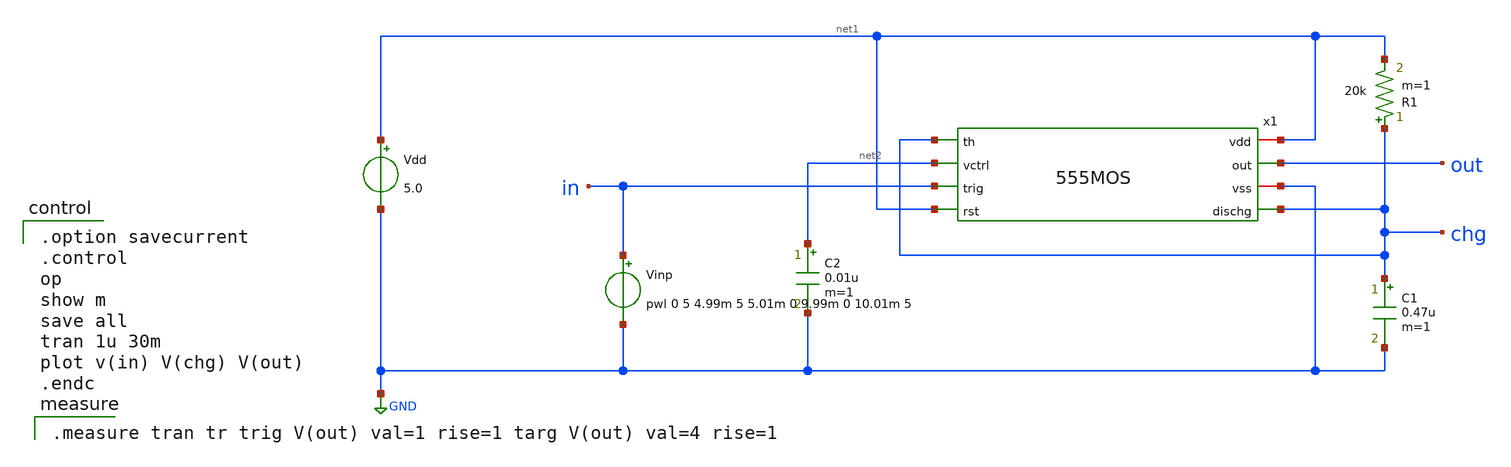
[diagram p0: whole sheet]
** sch_path: member_project/555timer/makoto645/555MOS_tran.sch
**.subckt 555MOS_tran
Vdd net1 GND 5.0
C1 chg GND 0.47u m=1
R1 chg net1 20k m=1
Vinp in GND pwl 0 5 4.99m 5 5.01m 0 9.99m 0 10.01m 5
x1 net1 chg out net2 in GND net1 chg 555MOS
C2 net2 GND 0.01u m=1
**** begin user architecture code

.option savecurrent
.control
op
show m
save all
tran 1u 30m
plot v(in) V(chg) V(out)
.endc


.measure tran tr trig V(out) val=1 rise=1 targ V(out) val=4 rise=1

 .include $::LIB/ip62_models
**** end user architecture code
**.ends

* expanding   symbol:  555MOS.sym # of pins=8
** sym_path: member_project/555timer/makoto645/555MOS.sym
** sch_path: member_project/555timer/makoto645/555MOS.sch
.subckt 555MOS vdd th out vctrl trig vss rst dischg
*.ipin vctrl
*.opin out
*.ipin trig
*.ipin th
*.ipin rst
*.opin dischg
*.iopin vdd
*.iopin vss
XM2 net2 vctrl net5 vss NMOS w=20u l=2u as=0 ad=0 ps=0 pd=0 nrd=0 nrs=0 m=1
XM1 net1 th net5 vss NMOS w=20u l=2u as=0 ad=0 ps=0 pd=0 nrd=0 nrs=0 m=1
XM3 net1 net1 vdd vdd PMOS w=20u l=2u as=0 ad=0 ps=0 pd=0 nrd=0 nrs=0 m=1
XM4 net4 net1 vdd vdd PMOS w=20u l=2u as=0 ad=0 ps=0 pd=0 nrd=0 nrs=0 m=1
XM5 net3 net2 vdd vdd PMOS w=20u l=2u as=0 ad=0 ps=0 pd=0 nrd=0 nrs=0 m=1
XM6 net2 net2 vdd vdd PMOS w=20u l=2u as=0 ad=0 ps=0 pd=0 nrd=0 nrs=0 m=1
XM7 net7 net11 net6 vdd PMOS w=80u l=2u as=0 ad=0 ps=0 pd=0 nrd=0 nrs=0 m=1
XR2 vdd net6 vdd F_RR w=6e-06 l=13.2e-06 R=1 tc1=0 tc2=0 m=1
XM8 net8 trig net7 vdd PMOS w=40u l=2u as=0 ad=0 ps=0 pd=0 nrd=0 nrs=0 m=1
XM9 net9 net10 net7 vdd PMOS w=40u l=2u as=0 ad=0 ps=0 pd=0 nrd=0 nrs=0 m=1
XM10 net8 net9 vss vss NMOS w=20u l=2u as=0 ad=0 ps=0 pd=0 nrd=0 nrs=0 m=1
XM11 net9 net9 vss vss NMOS w=20u l=2u as=0 ad=0 ps=0 pd=0 nrd=0 nrs=0 m=1
XR3 vdd vctrl vdd F_RR w=4e-06 l=42e-06 R=1 tc1=0 tc2=0 m=1
XR4 vctrl net10 vdd F_RR w=4e-06 l=42e-06 R=1 tc1=0 tc2=0 m=1
XR5 net10 vss vdd F_RR w=4e-06 l=42e-06 R=1 tc1=0 tc2=0 m=1
XM12 net3 net3 vss vss NMOS w=20u l=2u as=0 ad=0 ps=0 pd=0 nrd=0 nrs=0 m=1
XM13 net4 net3 vss vss NMOS w=20u l=2u as=0 ad=0 ps=0 pd=0 nrd=0 nrs=0 m=1
XM14 net11 net11 vdd vdd PMOS w=40u l=2u as=0 ad=0 ps=0 pd=0 nrd=0 nrs=0 m=1
XM15 net15 net11 vdd vdd PMOS w=40u l=2u as=0 ad=0 ps=0 pd=0 nrd=0 nrs=0 m=1
XM16 net12 net4 net13 vss NMOS w=20u l=2u as=0 ad=0 ps=0 pd=0 nrd=0 nrs=0 m=1
XM17 net12 net12 net14 vss NMOS w=20u l=2u as=0 ad=0 ps=0 pd=0 nrd=0 nrs=0 m=1
XR6 net11 net12 vdd F_RR w=4e-06 l=24.6e-06 R=1 tc1=0 tc2=0 m=1
XM18 net13 net8 vss vss NMOS w=20u l=2u as=0 ad=0 ps=0 pd=0 nrd=0 nrs=0 m=1
XM19 net14 net13 vss vss NMOS w=20u l=2u as=0 ad=0 ps=0 pd=0 nrd=0 nrs=0 m=1
XM20 net15 net14 vss vss NMOS w=20u l=2u as=0 ad=0 ps=0 pd=0 nrd=0 nrs=0 m=1
XM21 net16 net15 net18 vss NMOS w=20u l=2u as=0 ad=0 ps=0 pd=0 nrd=0 nrs=0 m=1
XR7 net15 net13 vdd F_RR w=4e-06 l=23.5e-06 R=1 tc1=0 tc2=0 m=1
XR8 vdd net16 vdd F_RR w=4e-06 l=24.6e-06 R=1 tc1=0 tc2=0 m=1
XM24 vdd net17 out vss NMOS w=40u l=2u as=0 ad=0 ps=0 pd=0 nrd=0 nrs=0 m=1
XM25 out net18 vss vss NMOS w=40u l=2u as=0 ad=0 ps=0 pd=0 nrd=0 nrs=0 m=1
XM22 vdd net16 net17 vss NMOS w=20u l=2u as=0 ad=0 ps=0 pd=0 nrd=0 nrs=0 m=1
XM23 vss net16 out vdd PMOS w=40u l=2u as=0 ad=0 ps=0 pd=0 nrd=0 nrs=0 m=1
XR9 net17 out vdd F_RR w=4e-06 l=24.6e-06 R=1 tc1=0 tc2=0 m=1
XR10 net18 vss vdd F_RR w=4e-06 l=24.6e-06 R=1 tc1=0 tc2=0 m=1
XM26 net18 rst net12 vdd PMOS w=40u l=2u as=0 ad=0 ps=0 pd=0 nrd=0 nrs=0 m=1
XM27 dischg net18 vss vss NMOS w=40u l=2u as=0 ad=0 ps=0 pd=0 nrd=0 nrs=0 m=1
XM28 net5 net19 vss vss NMOS w=40u l=2u as=0 ad=0 ps=0 pd=0 nrd=0 nrs=0 m=1
XR1 vdd net19 vdd F_RR w=4e-06 l=42e-06 R=1 tc1=0 tc2=0 m=1
XM29 net19 net19 vss vss NMOS w=40u l=2u as=0 ad=0 ps=0 pd=0 nrd=0 nrs=0 m=1
.ends

.GLOBAL GND
.end
